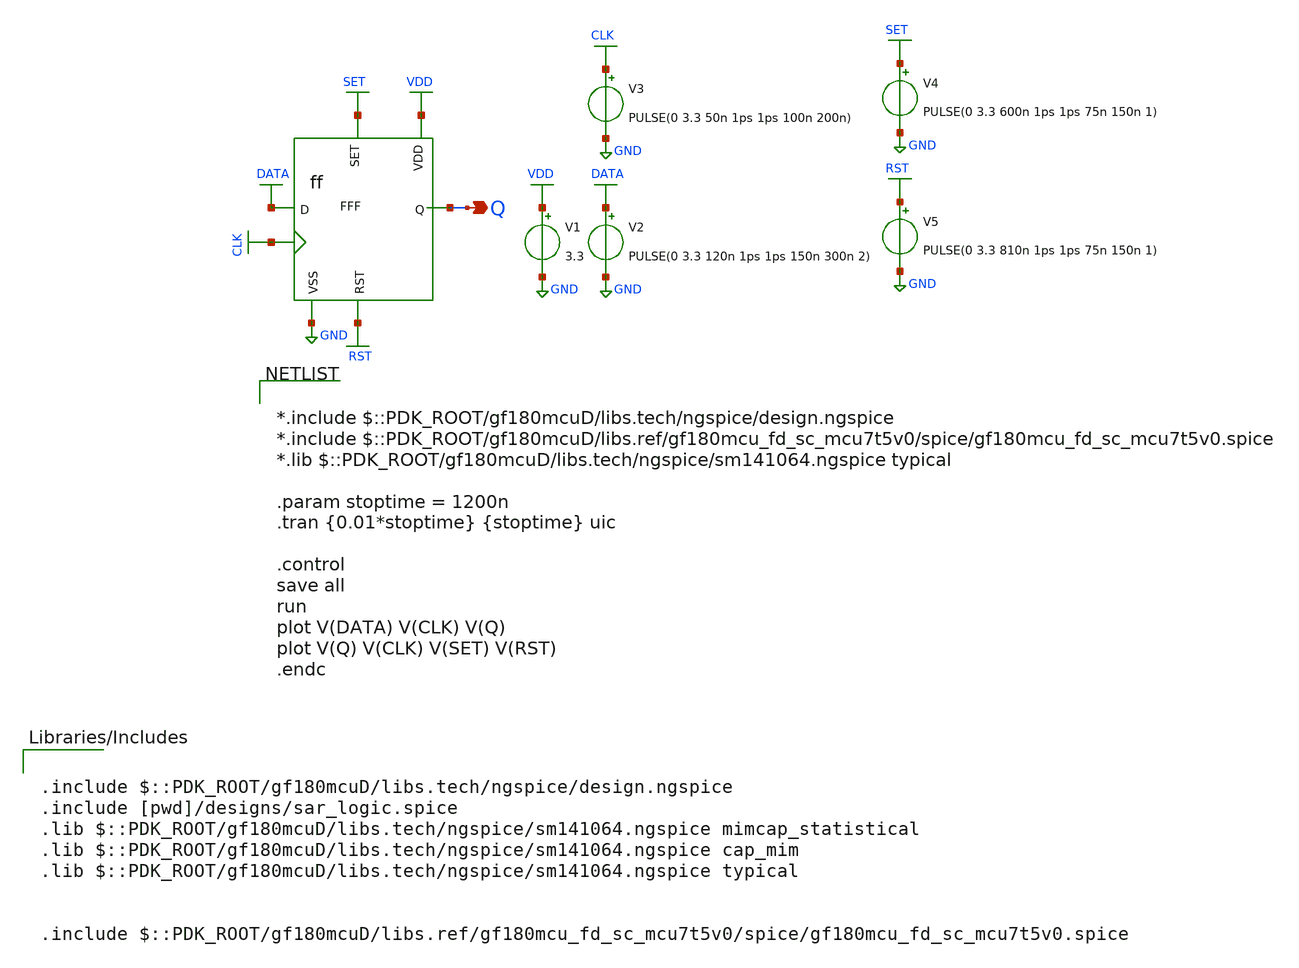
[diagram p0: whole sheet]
** sch_path: SAR_ADC/xschem/test/tb_ff.sch
**.subckt tb_ff Q
*.opin Q
V1 VDD GND 3.3
V2 DATA GND PULSE(0 3.3 120n 1ps 1ps 150n 300n 2)
V3 CLK GND PULSE(0 3.3 50n 1ps 1ps 100n 200n)
XFFF DATA RST SET CLK Q VDD GND GND GND gf180mcu_fd_sc_mcu7t5v0__dffrsnq_1
V4 SET GND PULSE(0 3.3 600n 1ps 1ps 75n 150n 1)
V5 RST GND PULSE(0 3.3 810n 1ps 1ps 75n 150n 1)
**** begin user architecture code


*.include $::PDK_ROOT/gf180mcuD/libs.tech/ngspice/design.ngspice
*.include $::PDK_ROOT/gf180mcuD/libs.ref/gf180mcu_fd_sc_mcu7t5v0/spice/gf180mcu_fd_sc_mcu7t5v0.spice
*.lib $::PDK_ROOT/gf180mcuD/libs.tech/ngspice/sm141064.ngspice typical

.param stoptime = 1200n
.tran {0.01*stoptime} {stoptime} uic

.control
save all
run
plot V(DATA) V(CLK) V(Q)
plot V(Q) V(CLK) V(SET) V(RST)
.endc



.include $::PDK_ROOT/gf180mcuD/libs.tech/ngspice/design.ngspice
.include [pwd]/designs/sar_logic.spice
.lib $::PDK_ROOT/gf180mcuD/libs.tech/ngspice/sm141064.ngspice mimcap_statistical
.lib $::PDK_ROOT/gf180mcuD/libs.tech/ngspice/sm141064.ngspice cap_mim
.lib $::PDK_ROOT/gf180mcuD/libs.tech/ngspice/sm141064.ngspice typical


.include $::PDK_ROOT/gf180mcuD/libs.ref/gf180mcu_fd_sc_mcu7t5v0/spice/gf180mcu_fd_sc_mcu7t5v0.spice


**** end user architecture code
**.ends
.GLOBAL DATA
.GLOBAL VDD
.GLOBAL GND
.GLOBAL CLK
.GLOBAL SET
.GLOBAL RST
.end
